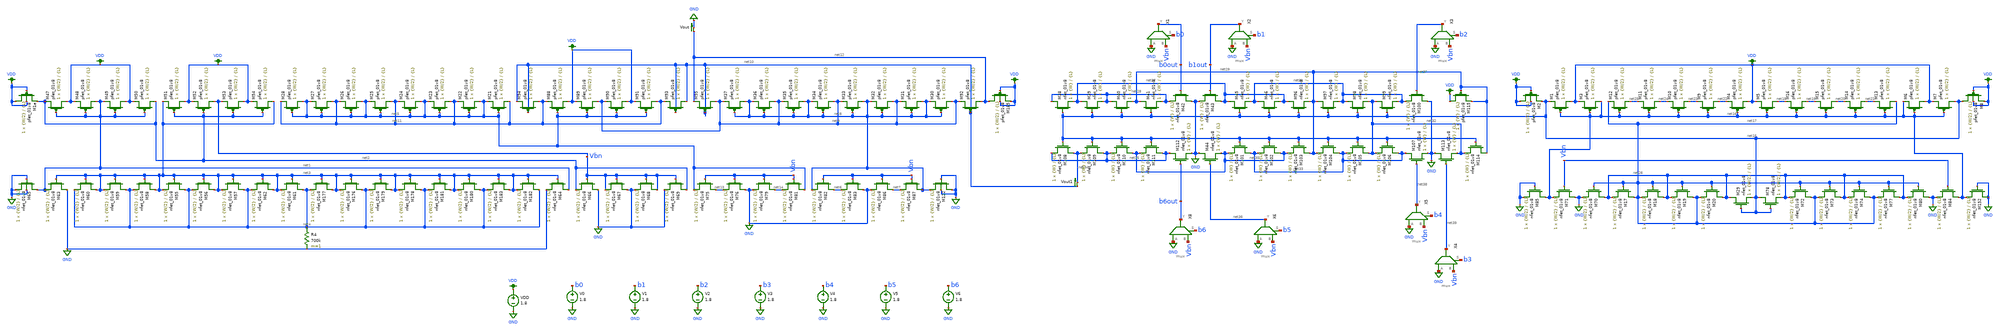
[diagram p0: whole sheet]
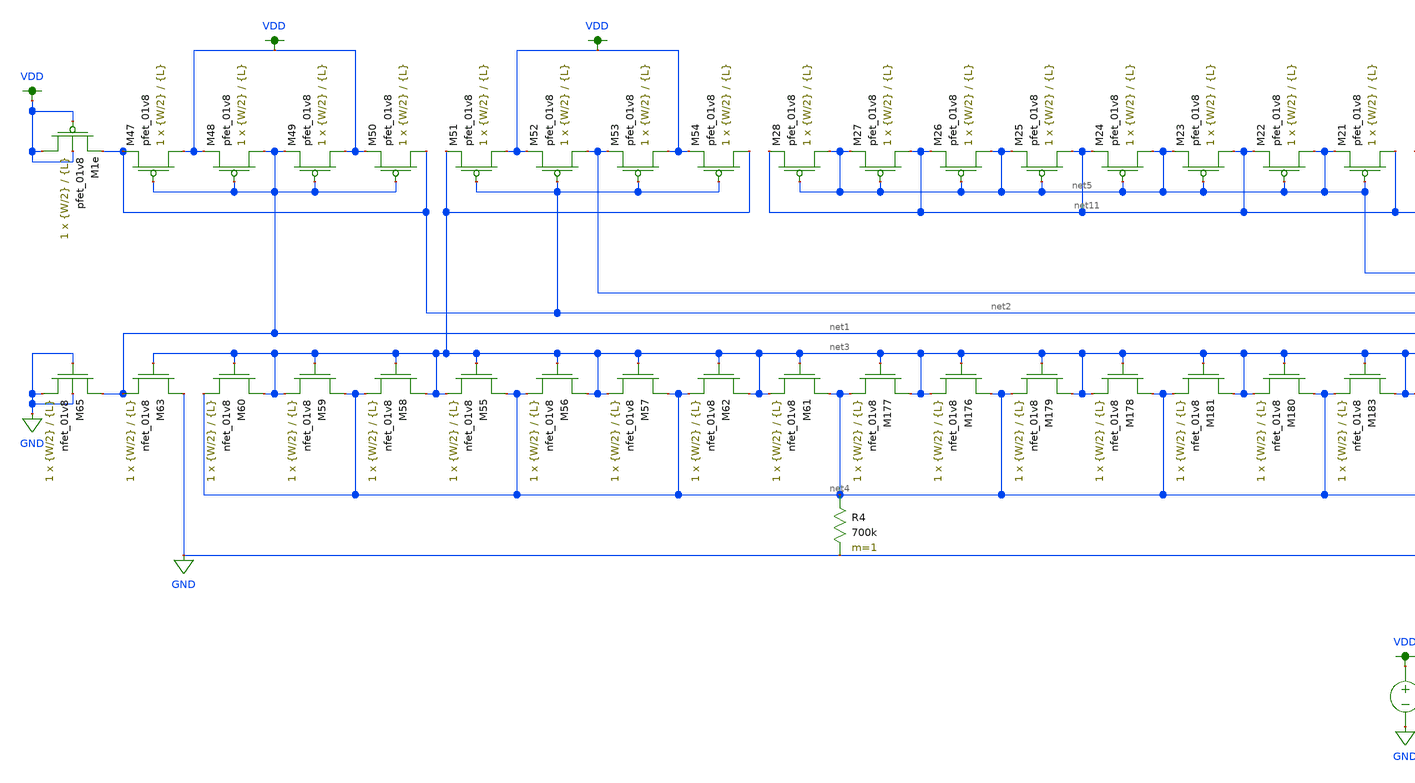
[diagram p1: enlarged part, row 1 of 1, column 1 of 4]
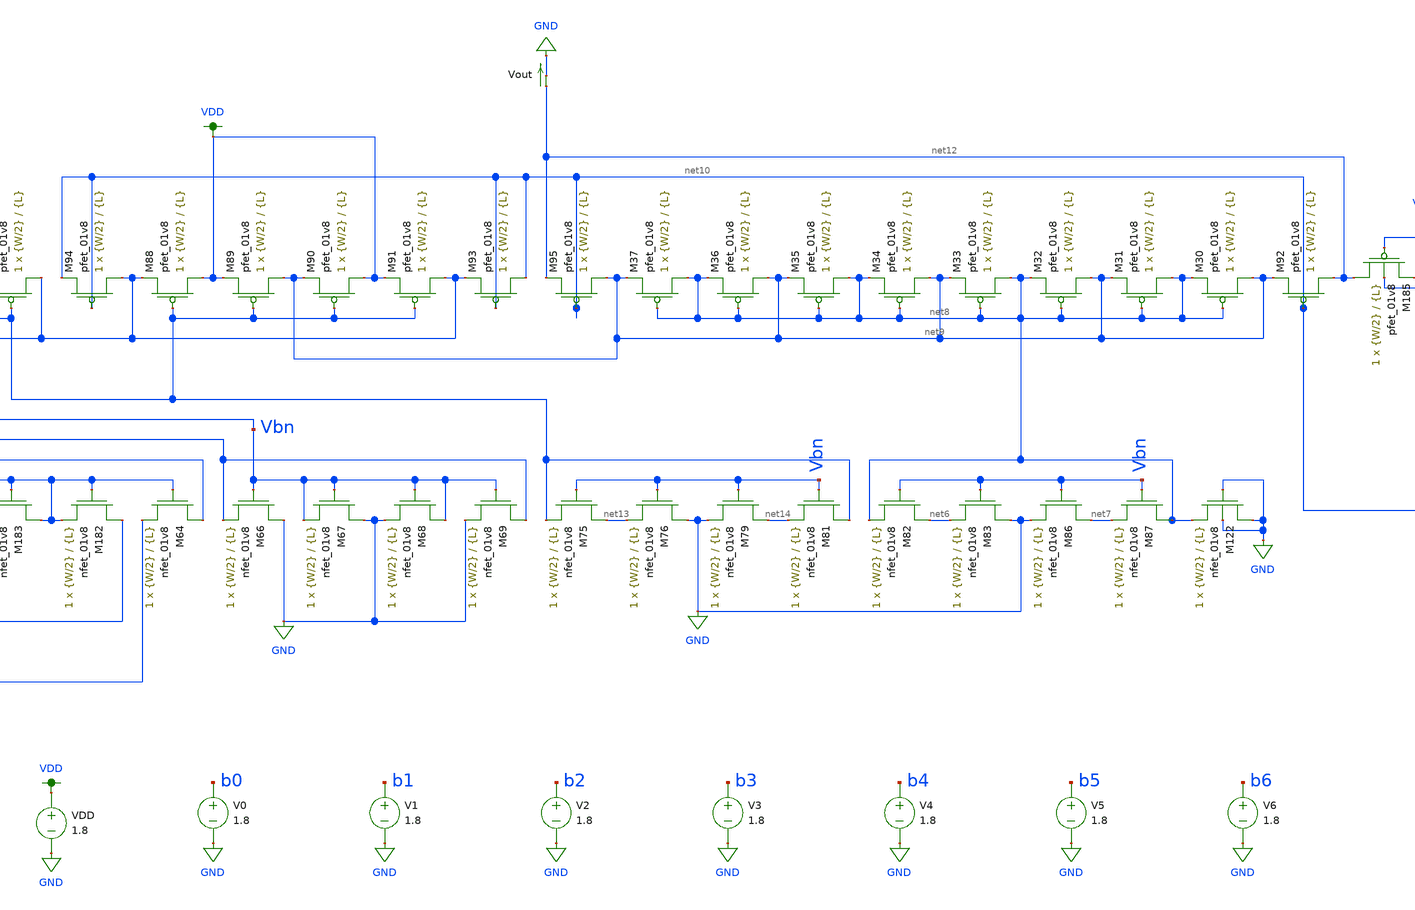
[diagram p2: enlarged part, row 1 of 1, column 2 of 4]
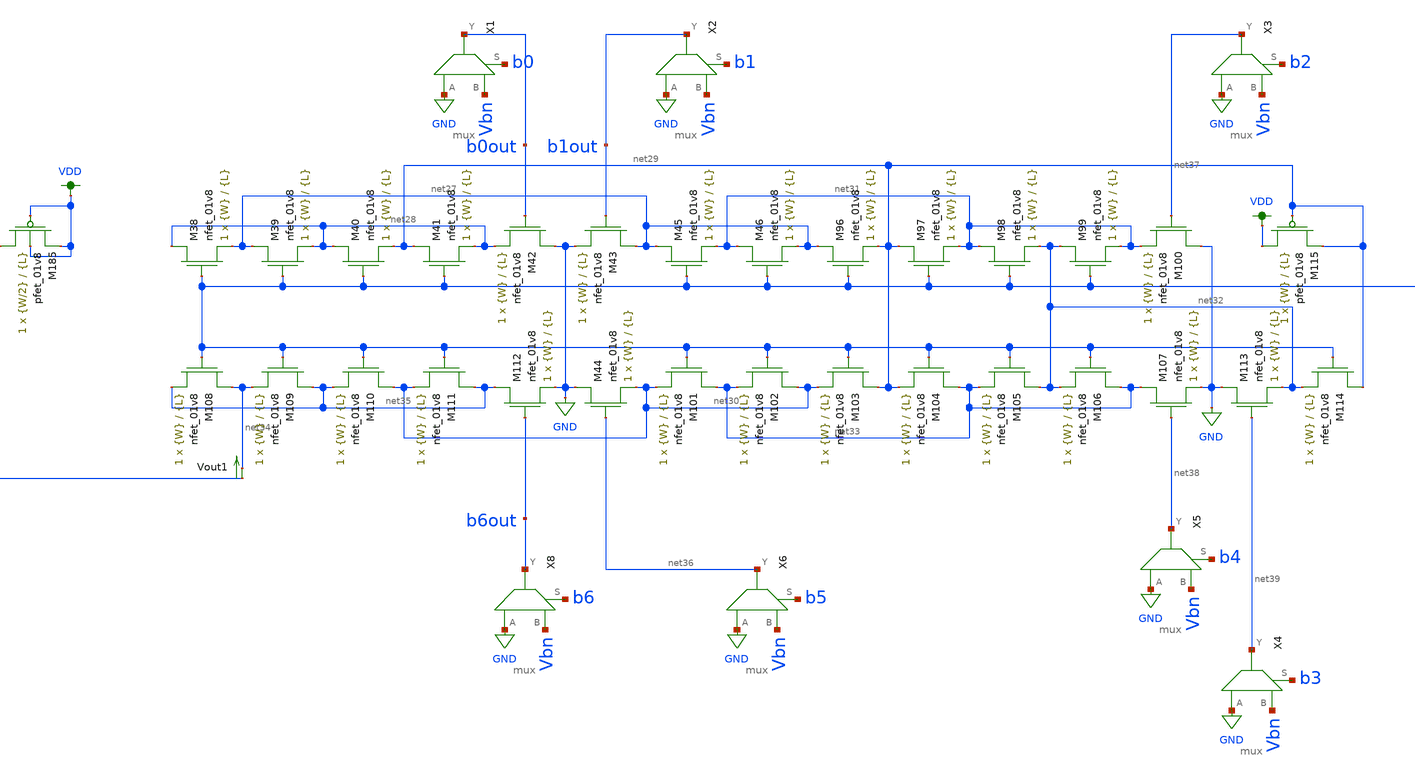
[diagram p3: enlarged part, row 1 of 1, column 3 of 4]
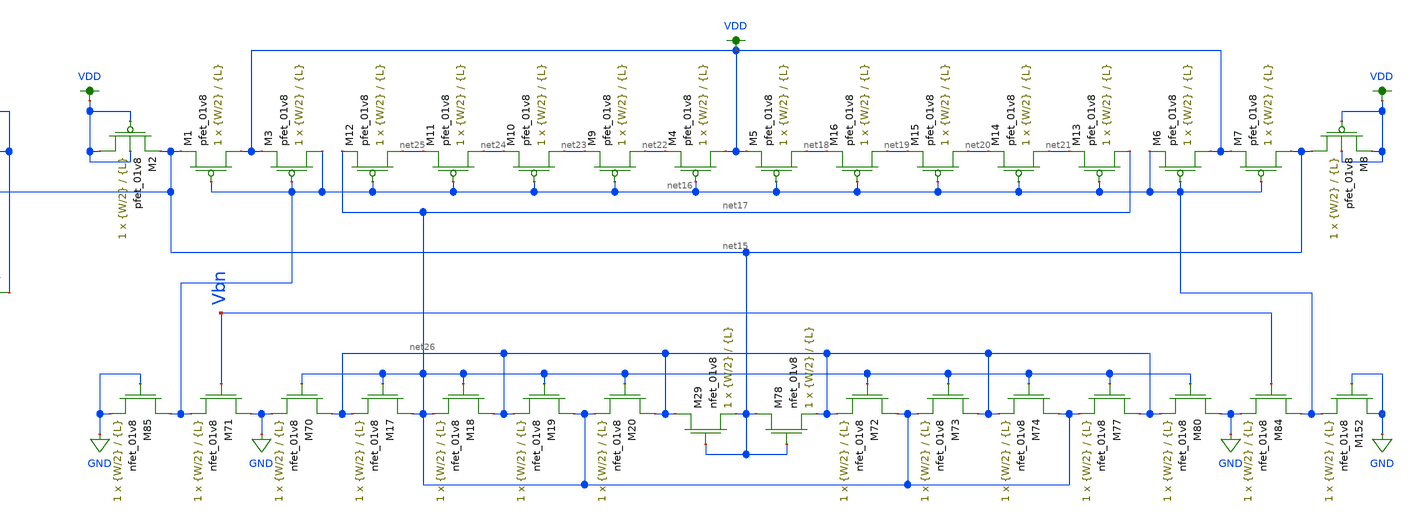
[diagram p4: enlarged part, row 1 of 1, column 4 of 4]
** sch_path: dac/schematics/LDS_FINAL_MONTE_CARLO.sch
**.subckt LDS_FINAL_MONTE_CARLO
V0 b0 GND 1.8
V1 b1 GND 1.8
V2 b2 GND 1.8
V3 b3 GND 1.8
V4 b4 GND 1.8
V5 b5 GND 1.8
V6 b6 GND 1.8
VDD VDD GND 1.8
XM47 VDD net1 net2 VDD sky130_fd_pr__pfet_01v8 L={L} W={W/2} nf=1 ad='int((nf+1)/2) * W/nf * 0.29' as='int((nf+2)/2) * W/nf * 0.29'
+ pd='2*int((nf+1)/2) * (W/nf + 0.29)' ps='2*int((nf+2)/2) * (W/nf + 0.29)' nrd='0.29 / W' nrs='0.29 / W'
+ sa=0 sb=0 sd=0 mult=1 m=1
XM48 net1 net1 VDD VDD sky130_fd_pr__pfet_01v8 L={L} W={W/2} nf=1 ad='int((nf+1)/2) * W/nf * 0.29' as='int((nf+2)/2) * W/nf * 0.29'
+ pd='2*int((nf+1)/2) * (W/nf + 0.29)' ps='2*int((nf+2)/2) * (W/nf + 0.29)' nrd='0.29 / W' nrs='0.29 / W'
+ sa=0 sb=0 sd=0 mult=1 m=1
XM49 VDD net1 net1 VDD sky130_fd_pr__pfet_01v8 L={L} W={W/2} nf=1 ad='int((nf+1)/2) * W/nf * 0.29' as='int((nf+2)/2) * W/nf * 0.29'
+ pd='2*int((nf+1)/2) * (W/nf + 0.29)' ps='2*int((nf+2)/2) * (W/nf + 0.29)' nrd='0.29 / W' nrs='0.29 / W'
+ sa=0 sb=0 sd=0 mult=1 m=1
XM50 net2 net1 VDD VDD sky130_fd_pr__pfet_01v8 L={L} W={W/2} nf=1 ad='int((nf+1)/2) * W/nf * 0.29' as='int((nf+2)/2) * W/nf * 0.29'
+ pd='2*int((nf+1)/2) * (W/nf + 0.29)' ps='2*int((nf+2)/2) * (W/nf + 0.29)' nrd='0.29 / W' nrs='0.29 / W'
+ sa=0 sb=0 sd=0 mult=1 m=1
XM51 VDD net2 net3 VDD sky130_fd_pr__pfet_01v8 L={L} W={W/2} nf=1 ad='int((nf+1)/2) * W/nf * 0.29' as='int((nf+2)/2) * W/nf * 0.29'
+ pd='2*int((nf+1)/2) * (W/nf + 0.29)' ps='2*int((nf+2)/2) * (W/nf + 0.29)' nrd='0.29 / W' nrs='0.29 / W'
+ sa=0 sb=0 sd=0 mult=1 m=1
XM52 Vbn net2 VDD VDD sky130_fd_pr__pfet_01v8 L={L} W={W/2} nf=1 ad='int((nf+1)/2) * W/nf * 0.29' as='int((nf+2)/2) * W/nf * 0.29'
+ pd='2*int((nf+1)/2) * (W/nf + 0.29)' ps='2*int((nf+2)/2) * (W/nf + 0.29)' nrd='0.29 / W' nrs='0.29 / W'
+ sa=0 sb=0 sd=0 mult=1 m=1
XM53 VDD net2 Vbn VDD sky130_fd_pr__pfet_01v8 L={L} W={W/2} nf=1 ad='int((nf+1)/2) * W/nf * 0.29' as='int((nf+2)/2) * W/nf * 0.29'
+ pd='2*int((nf+1)/2) * (W/nf + 0.29)' ps='2*int((nf+2)/2) * (W/nf + 0.29)' nrd='0.29 / W' nrs='0.29 / W'
+ sa=0 sb=0 sd=0 mult=1 m=1
XM54 net3 net2 VDD VDD sky130_fd_pr__pfet_01v8 L={L} W={W/2} nf=1 ad='int((nf+1)/2) * W/nf * 0.29' as='int((nf+2)/2) * W/nf * 0.29'
+ pd='2*int((nf+1)/2) * (W/nf + 0.29)' ps='2*int((nf+2)/2) * (W/nf + 0.29)' nrd='0.29 / W' nrs='0.29 / W'
+ sa=0 sb=0 sd=0 mult=1 m=1
XM55 net4 net3 net3 GND sky130_fd_pr__nfet_01v8 L={L} W={W/2} nf=1 ad='int((nf+1)/2) * W/nf * 0.29' as='int((nf+2)/2) * W/nf * 0.29'
+ pd='2*int((nf+1)/2) * (W/nf + 0.29)' ps='2*int((nf+2)/2) * (W/nf + 0.29)' nrd='0.29 / W' nrs='0.29 / W'
+ sa=0 sb=0 sd=0 mult=1 m=1
XM56 net3 net3 net4 GND sky130_fd_pr__nfet_01v8 L={L} W={W/2} nf=1 ad='int((nf+1)/2) * W/nf * 0.29' as='int((nf+2)/2) * W/nf * 0.29'
+ pd='2*int((nf+1)/2) * (W/nf + 0.29)' ps='2*int((nf+2)/2) * (W/nf + 0.29)' nrd='0.29 / W' nrs='0.29 / W'
+ sa=0 sb=0 sd=0 mult=1 m=1
XM57 net4 net3 net3 GND sky130_fd_pr__nfet_01v8 L={L} W={W/2} nf=1 ad='int((nf+1)/2) * W/nf * 0.29' as='int((nf+2)/2) * W/nf * 0.29'
+ pd='2*int((nf+1)/2) * (W/nf + 0.29)' ps='2*int((nf+2)/2) * (W/nf + 0.29)' nrd='0.29 / W' nrs='0.29 / W'
+ sa=0 sb=0 sd=0 mult=1 m=1
XM58 net3 net3 net4 GND sky130_fd_pr__nfet_01v8 L={L} W={W/2} nf=1 ad='int((nf+1)/2) * W/nf * 0.29' as='int((nf+2)/2) * W/nf * 0.29'
+ pd='2*int((nf+1)/2) * (W/nf + 0.29)' ps='2*int((nf+2)/2) * (W/nf + 0.29)' nrd='0.29 / W' nrs='0.29 / W'
+ sa=0 sb=0 sd=0 mult=1 m=1
XM59 net4 net3 net3 GND sky130_fd_pr__nfet_01v8 L={L} W={W/2} nf=1 ad='int((nf+1)/2) * W/nf * 0.29' as='int((nf+2)/2) * W/nf * 0.29'
+ pd='2*int((nf+1)/2) * (W/nf + 0.29)' ps='2*int((nf+2)/2) * (W/nf + 0.29)' nrd='0.29 / W' nrs='0.29 / W'
+ sa=0 sb=0 sd=0 mult=1 m=1
XM60 net3 net3 net4 GND sky130_fd_pr__nfet_01v8 L={L} W={W/2} nf=1 ad='int((nf+1)/2) * W/nf * 0.29' as='int((nf+2)/2) * W/nf * 0.29'
+ pd='2*int((nf+1)/2) * (W/nf + 0.29)' ps='2*int((nf+2)/2) * (W/nf + 0.29)' nrd='0.29 / W' nrs='0.29 / W'
+ sa=0 sb=0 sd=0 mult=1 m=1
XM61 net4 net3 net3 GND sky130_fd_pr__nfet_01v8 L={L} W={W/2} nf=1 ad='int((nf+1)/2) * W/nf * 0.29' as='int((nf+2)/2) * W/nf * 0.29'
+ pd='2*int((nf+1)/2) * (W/nf + 0.29)' ps='2*int((nf+2)/2) * (W/nf + 0.29)' nrd='0.29 / W' nrs='0.29 / W'
+ sa=0 sb=0 sd=0 mult=1 m=1
XM62 net3 net3 net4 GND sky130_fd_pr__nfet_01v8 L={L} W={W/2} nf=1 ad='int((nf+1)/2) * W/nf * 0.29' as='int((nf+2)/2) * W/nf * 0.29'
+ pd='2*int((nf+1)/2) * (W/nf + 0.29)' ps='2*int((nf+2)/2) * (W/nf + 0.29)' nrd='0.29 / W' nrs='0.29 / W'
+ sa=0 sb=0 sd=0 mult=1 m=1
XM63 GND net3 net1 GND sky130_fd_pr__nfet_01v8 L={L} W={W/2} nf=1 ad='int((nf+1)/2) * W/nf * 0.29' as='int((nf+2)/2) * W/nf * 0.29'
+ pd='2*int((nf+1)/2) * (W/nf + 0.29)' ps='2*int((nf+2)/2) * (W/nf + 0.29)' nrd='0.29 / W' nrs='0.29 / W'
+ sa=0 sb=0 sd=0 mult=1 m=1
XM64 net1 net3 GND GND sky130_fd_pr__nfet_01v8 L={L} W={W/2} nf=1 ad='int((nf+1)/2) * W/nf * 0.29' as='int((nf+2)/2) * W/nf * 0.29'
+ pd='2*int((nf+1)/2) * (W/nf + 0.29)' ps='2*int((nf+2)/2) * (W/nf + 0.29)' nrd='0.29 / W' nrs='0.29 / W'
+ sa=0 sb=0 sd=0 mult=1 m=1
R4 net4 GND 700k m=1
XM1e VDD VDD net2 VDD sky130_fd_pr__pfet_01v8 L={L} W={W/2} nf=1 ad='int((nf+1)/2) * W/nf * 0.29' as='int((nf+2)/2) * W/nf * 0.29'
+ pd='2*int((nf+1)/2) * (W/nf + 0.29)' ps='2*int((nf+2)/2) * (W/nf + 0.29)' nrd='0.29 / W' nrs='0.29 / W'
+ sa=0 sb=0 sd=0 mult=1 m=1
XM65 net1 GND GND GND sky130_fd_pr__nfet_01v8 L={L} W={W/2} nf=1 ad='int((nf+1)/2) * W/nf * 0.29' as='int((nf+2)/2) * W/nf * 0.29'
+ pd='2*int((nf+1)/2) * (W/nf + 0.29)' ps='2*int((nf+2)/2) * (W/nf + 0.29)' nrd='0.29 / W' nrs='0.29 / W'
+ sa=0 sb=0 sd=0 mult=1 m=1
XM66 GND Vbn net2 GND sky130_fd_pr__nfet_01v8 L={L} W={W/2} nf=1 ad='int((nf+1)/2) * W/nf * 0.29' as='int((nf+2)/2) * W/nf * 0.29'
+ pd='2*int((nf+1)/2) * (W/nf + 0.29)' ps='2*int((nf+2)/2) * (W/nf + 0.29)' nrd='0.29 / W' nrs='0.29 / W'
+ sa=0 sb=0 sd=0 mult=1 m=1
XM67 GND Vbn Vbn GND sky130_fd_pr__nfet_01v8 L={L} W={W/2} nf=1 ad='int((nf+1)/2) * W/nf * 0.29' as='int((nf+2)/2) * W/nf * 0.29'
+ pd='2*int((nf+1)/2) * (W/nf + 0.29)' ps='2*int((nf+2)/2) * (W/nf + 0.29)' nrd='0.29 / W' nrs='0.29 / W'
+ sa=0 sb=0 sd=0 mult=1 m=1
XM68 Vbn Vbn GND GND sky130_fd_pr__nfet_01v8 L={L} W={W/2} nf=1 ad='int((nf+1)/2) * W/nf * 0.29' as='int((nf+2)/2) * W/nf * 0.29'
+ pd='2*int((nf+1)/2) * (W/nf + 0.29)' ps='2*int((nf+2)/2) * (W/nf + 0.29)' nrd='0.29 / W' nrs='0.29 / W'
+ sa=0 sb=0 sd=0 mult=1 m=1
XM69 net2 Vbn GND GND sky130_fd_pr__nfet_01v8 L={L} W={W/2} nf=1 ad='int((nf+1)/2) * W/nf * 0.29' as='int((nf+2)/2) * W/nf * 0.29'
+ pd='2*int((nf+1)/2) * (W/nf + 0.29)' ps='2*int((nf+2)/2) * (W/nf + 0.29)' nrd='0.29 / W' nrs='0.29 / W'
+ sa=0 sb=0 sd=0 mult=1 m=1
XM75 net13 Vbn net5 GND sky130_fd_pr__nfet_01v8 L={L} W={W/2} nf=1 ad='int((nf+1)/2) * W/nf * 0.29' as='int((nf+2)/2) * W/nf * 0.29'
+ pd='2*int((nf+1)/2) * (W/nf + 0.29)' ps='2*int((nf+2)/2) * (W/nf + 0.29)' nrd='0.29 / W' nrs='0.29 / W'
+ sa=0 sb=0 sd=0 mult=1 m=1
XM76 GND Vbn net13 GND sky130_fd_pr__nfet_01v8 L={L} W={W/2} nf=1 ad='int((nf+1)/2) * W/nf * 0.29' as='int((nf+2)/2) * W/nf * 0.29'
+ pd='2*int((nf+1)/2) * (W/nf + 0.29)' ps='2*int((nf+2)/2) * (W/nf + 0.29)' nrd='0.29 / W' nrs='0.29 / W'
+ sa=0 sb=0 sd=0 mult=1 m=1
XM79 net14 Vbn GND GND sky130_fd_pr__nfet_01v8 L={L} W={W/2} nf=1 ad='int((nf+1)/2) * W/nf * 0.29' as='int((nf+2)/2) * W/nf * 0.29'
+ pd='2*int((nf+1)/2) * (W/nf + 0.29)' ps='2*int((nf+2)/2) * (W/nf + 0.29)' nrd='0.29 / W' nrs='0.29 / W'
+ sa=0 sb=0 sd=0 mult=1 m=1
XM81 net5 Vbn net14 GND sky130_fd_pr__nfet_01v8 L={L} W={W/2} nf=1 ad='int((nf+1)/2) * W/nf * 0.29' as='int((nf+2)/2) * W/nf * 0.29'
+ pd='2*int((nf+1)/2) * (W/nf + 0.29)' ps='2*int((nf+2)/2) * (W/nf + 0.29)' nrd='0.29 / W' nrs='0.29 / W'
+ sa=0 sb=0 sd=0 mult=1 m=1
XM82 net6 Vbn net8 GND sky130_fd_pr__nfet_01v8 L={L} W={W/2} nf=1 ad='int((nf+1)/2) * W/nf * 0.29' as='int((nf+2)/2) * W/nf * 0.29'
+ pd='2*int((nf+1)/2) * (W/nf + 0.29)' ps='2*int((nf+2)/2) * (W/nf + 0.29)' nrd='0.29 / W' nrs='0.29 / W'
+ sa=0 sb=0 sd=0 mult=1 m=1
XM83 GND Vbn net6 GND sky130_fd_pr__nfet_01v8 L={L} W={W/2} nf=1 ad='int((nf+1)/2) * W/nf * 0.29' as='int((nf+2)/2) * W/nf * 0.29'
+ pd='2*int((nf+1)/2) * (W/nf + 0.29)' ps='2*int((nf+2)/2) * (W/nf + 0.29)' nrd='0.29 / W' nrs='0.29 / W'
+ sa=0 sb=0 sd=0 mult=1 m=1
XM86 net7 Vbn GND GND sky130_fd_pr__nfet_01v8 L={L} W={W/2} nf=1 ad='int((nf+1)/2) * W/nf * 0.29' as='int((nf+2)/2) * W/nf * 0.29'
+ pd='2*int((nf+1)/2) * (W/nf + 0.29)' ps='2*int((nf+2)/2) * (W/nf + 0.29)' nrd='0.29 / W' nrs='0.29 / W'
+ sa=0 sb=0 sd=0 mult=1 m=1
XM87 net8 Vbn net7 GND sky130_fd_pr__nfet_01v8 L={L} W={W/2} nf=1 ad='int((nf+1)/2) * W/nf * 0.29' as='int((nf+2)/2) * W/nf * 0.29'
+ pd='2*int((nf+1)/2) * (W/nf + 0.29)' ps='2*int((nf+2)/2) * (W/nf + 0.29)' nrd='0.29 / W' nrs='0.29 / W'
+ sa=0 sb=0 sd=0 mult=1 m=1
XM88 VDD net5 net11 VDD sky130_fd_pr__pfet_01v8 L={L} W={W/2} nf=1 ad='int((nf+1)/2) * W/nf * 0.29' as='int((nf+2)/2) * W/nf * 0.29'
+ pd='2*int((nf+1)/2) * (W/nf + 0.29)' ps='2*int((nf+2)/2) * (W/nf + 0.29)' nrd='0.29 / W' nrs='0.29 / W'
+ sa=0 sb=0 sd=0 mult=1 m=1
XM89 net9 net5 VDD VDD sky130_fd_pr__pfet_01v8 L={L} W={W/2} nf=1 ad='int((nf+1)/2) * W/nf * 0.29' as='int((nf+2)/2) * W/nf * 0.29'
+ pd='2*int((nf+1)/2) * (W/nf + 0.29)' ps='2*int((nf+2)/2) * (W/nf + 0.29)' nrd='0.29 / W' nrs='0.29 / W'
+ sa=0 sb=0 sd=0 mult=1 m=1
XM90 VDD net5 net9 VDD sky130_fd_pr__pfet_01v8 L={L} W={W/2} nf=1 ad='int((nf+1)/2) * W/nf * 0.29' as='int((nf+2)/2) * W/nf * 0.29'
+ pd='2*int((nf+1)/2) * (W/nf + 0.29)' ps='2*int((nf+2)/2) * (W/nf + 0.29)' nrd='0.29 / W' nrs='0.29 / W'
+ sa=0 sb=0 sd=0 mult=1 m=1
XM91 net11 net5 VDD VDD sky130_fd_pr__pfet_01v8 L={L} W={W/2} nf=1 ad='int((nf+1)/2) * W/nf * 0.29' as='int((nf+2)/2) * W/nf * 0.29'
+ pd='2*int((nf+1)/2) * (W/nf + 0.29)' ps='2*int((nf+2)/2) * (W/nf + 0.29)' nrd='0.29 / W' nrs='0.29 / W'
+ sa=0 sb=0 sd=0 mult=1 m=1
XM92 net12 net10 net9 VDD sky130_fd_pr__pfet_01v8 L={L} W={W/2} nf=1 ad='int((nf+1)/2) * W/nf * 0.29'
+ as='int((nf+2)/2) * W/nf * 0.29' pd='2*int((nf+1)/2) * (W/nf + 0.29)' ps='2*int((nf+2)/2) * (W/nf + 0.29)'
+ nrd='0.29 / W' nrs='0.29 / W' sa=0 sb=0 sd=0 mult=1 m=1
XM93 net10 net10 net11 VDD sky130_fd_pr__pfet_01v8 L={L} W={W/2} nf=1 ad='int((nf+1)/2) * W/nf * 0.29'
+ as='int((nf+2)/2) * W/nf * 0.29' pd='2*int((nf+1)/2) * (W/nf + 0.29)' ps='2*int((nf+2)/2) * (W/nf + 0.29)'
+ nrd='0.29 / W' nrs='0.29 / W' sa=0 sb=0 sd=0 mult=1 m=1
XM94 net11 net10 net10 VDD sky130_fd_pr__pfet_01v8 L={L} W={W/2} nf=1 ad='int((nf+1)/2) * W/nf * 0.29'
+ as='int((nf+2)/2) * W/nf * 0.29' pd='2*int((nf+1)/2) * (W/nf + 0.29)' ps='2*int((nf+2)/2) * (W/nf + 0.29)'
+ nrd='0.29 / W' nrs='0.29 / W' sa=0 sb=0 sd=0 mult=1 m=1
XM95 net9 net10 net12 VDD sky130_fd_pr__pfet_01v8 L={L} W={W/2} nf=1 ad='int((nf+1)/2) * W/nf * 0.29'
+ as='int((nf+2)/2) * W/nf * 0.29' pd='2*int((nf+1)/2) * (W/nf + 0.29)' ps='2*int((nf+2)/2) * (W/nf + 0.29)'
+ nrd='0.29 / W' nrs='0.29 / W' sa=0 sb=0 sd=0 mult=1 m=1
XM176 net4 net3 net3 GND sky130_fd_pr__nfet_01v8 L={L} W={W/2} nf=1 ad='int((nf+1)/2) * W/nf * 0.29'
+ as='int((nf+2)/2) * W/nf * 0.29' pd='2*int((nf+1)/2) * (W/nf + 0.29)' ps='2*int((nf+2)/2) * (W/nf + 0.29)'
+ nrd='0.29 / W' nrs='0.29 / W' sa=0 sb=0 sd=0 mult=1 m=1
XM177 net3 net3 net4 GND sky130_fd_pr__nfet_01v8 L={L} W={W/2} nf=1 ad='int((nf+1)/2) * W/nf * 0.29'
+ as='int((nf+2)/2) * W/nf * 0.29' pd='2*int((nf+1)/2) * (W/nf + 0.29)' ps='2*int((nf+2)/2) * (W/nf + 0.29)'
+ nrd='0.29 / W' nrs='0.29 / W' sa=0 sb=0 sd=0 mult=1 m=1
XM178 net4 net3 net3 GND sky130_fd_pr__nfet_01v8 L={L} W={W/2} nf=1 ad='int((nf+1)/2) * W/nf * 0.29'
+ as='int((nf+2)/2) * W/nf * 0.29' pd='2*int((nf+1)/2) * (W/nf + 0.29)' ps='2*int((nf+2)/2) * (W/nf + 0.29)'
+ nrd='0.29 / W' nrs='0.29 / W' sa=0 sb=0 sd=0 mult=1 m=1
XM179 net3 net3 net4 GND sky130_fd_pr__nfet_01v8 L={L} W={W/2} nf=1 ad='int((nf+1)/2) * W/nf * 0.29'
+ as='int((nf+2)/2) * W/nf * 0.29' pd='2*int((nf+1)/2) * (W/nf + 0.29)' ps='2*int((nf+2)/2) * (W/nf + 0.29)'
+ nrd='0.29 / W' nrs='0.29 / W' sa=0 sb=0 sd=0 mult=1 m=1
XM180 net4 net3 net3 GND sky130_fd_pr__nfet_01v8 L={L} W={W/2} nf=1 ad='int((nf+1)/2) * W/nf * 0.29'
+ as='int((nf+2)/2) * W/nf * 0.29' pd='2*int((nf+1)/2) * (W/nf + 0.29)' ps='2*int((nf+2)/2) * (W/nf + 0.29)'
+ nrd='0.29 / W' nrs='0.29 / W' sa=0 sb=0 sd=0 mult=1 m=1
XM181 net3 net3 net4 GND sky130_fd_pr__nfet_01v8 L={L} W={W/2} nf=1 ad='int((nf+1)/2) * W/nf * 0.29'
+ as='int((nf+2)/2) * W/nf * 0.29' pd='2*int((nf+1)/2) * (W/nf + 0.29)' ps='2*int((nf+2)/2) * (W/nf + 0.29)'
+ nrd='0.29 / W' nrs='0.29 / W' sa=0 sb=0 sd=0 mult=1 m=1
XM182 net4 net3 net3 GND sky130_fd_pr__nfet_01v8 L={L} W={W/2} nf=1 ad='int((nf+1)/2) * W/nf * 0.29'
+ as='int((nf+2)/2) * W/nf * 0.29' pd='2*int((nf+1)/2) * (W/nf + 0.29)' ps='2*int((nf+2)/2) * (W/nf + 0.29)'
+ nrd='0.29 / W' nrs='0.29 / W' sa=0 sb=0 sd=0 mult=1 m=1
XM183 net3 net3 net4 GND sky130_fd_pr__nfet_01v8 L={L} W={W/2} nf=1 ad='int((nf+1)/2) * W/nf * 0.29'
+ as='int((nf+2)/2) * W/nf * 0.29' pd='2*int((nf+1)/2) * (W/nf + 0.29)' ps='2*int((nf+2)/2) * (W/nf + 0.29)'
+ nrd='0.29 / W' nrs='0.29 / W' sa=0 sb=0 sd=0 mult=1 m=1
XM185 net12 VDD VDD VDD sky130_fd_pr__pfet_01v8 L={L} W={W/2} nf=1 ad='int((nf+1)/2) * W/nf * 0.29' as='int((nf+2)/2) * W/nf * 0.29'
+ pd='2*int((nf+1)/2) * (W/nf + 0.29)' ps='2*int((nf+2)/2) * (W/nf + 0.29)' nrd='0.29 / W' nrs='0.29 / W'
+ sa=0 sb=0 sd=0 mult=1 m=1
Vout net12 GND 0
.save i(vout)
XM21 net11 net5 net5 VDD sky130_fd_pr__pfet_01v8 L={L} W={W/2} nf=1 ad='int((nf+1)/2) * W/nf * 0.29'
+ as='int((nf+2)/2) * W/nf * 0.29' pd='2*int((nf+1)/2) * (W/nf + 0.29)' ps='2*int((nf+2)/2) * (W/nf + 0.29)'
+ nrd='0.29 / W' nrs='0.29 / W' sa=0 sb=0 sd=0 mult=1 m=1
XM22 net5 net5 net11 VDD sky130_fd_pr__pfet_01v8 L={L} W={W/2} nf=1 ad='int((nf+1)/2) * W/nf * 0.29'
+ as='int((nf+2)/2) * W/nf * 0.29' pd='2*int((nf+1)/2) * (W/nf + 0.29)' ps='2*int((nf+2)/2) * (W/nf + 0.29)'
+ nrd='0.29 / W' nrs='0.29 / W' sa=0 sb=0 sd=0 mult=1 m=1
XM23 net11 net5 net5 VDD sky130_fd_pr__pfet_01v8 L={L} W={W/2} nf=1 ad='int((nf+1)/2) * W/nf * 0.29'
+ as='int((nf+2)/2) * W/nf * 0.29' pd='2*int((nf+1)/2) * (W/nf + 0.29)' ps='2*int((nf+2)/2) * (W/nf + 0.29)'
+ nrd='0.29 / W' nrs='0.29 / W' sa=0 sb=0 sd=0 mult=1 m=1
XM24 net5 net5 net11 VDD sky130_fd_pr__pfet_01v8 L={L} W={W/2} nf=1 ad='int((nf+1)/2) * W/nf * 0.29'
+ as='int((nf+2)/2) * W/nf * 0.29' pd='2*int((nf+1)/2) * (W/nf + 0.29)' ps='2*int((nf+2)/2) * (W/nf + 0.29)'
+ nrd='0.29 / W' nrs='0.29 / W' sa=0 sb=0 sd=0 mult=1 m=1
XM25 net11 net5 net5 VDD sky130_fd_pr__pfet_01v8 L={L} W={W/2} nf=1 ad='int((nf+1)/2) * W/nf * 0.29'
+ as='int((nf+2)/2) * W/nf * 0.29' pd='2*int((nf+1)/2) * (W/nf + 0.29)' ps='2*int((nf+2)/2) * (W/nf + 0.29)'
+ nrd='0.29 / W' nrs='0.29 / W' sa=0 sb=0 sd=0 mult=1 m=1
XM26 net5 net5 net11 VDD sky130_fd_pr__pfet_01v8 L={L} W={W/2} nf=1 ad='int((nf+1)/2) * W/nf * 0.29'
+ as='int((nf+2)/2) * W/nf * 0.29' pd='2*int((nf+1)/2) * (W/nf + 0.29)' ps='2*int((nf+2)/2) * (W/nf + 0.29)'
+ nrd='0.29 / W' nrs='0.29 / W' sa=0 sb=0 sd=0 mult=1 m=1
XM27 net11 net5 net5 VDD sky130_fd_pr__pfet_01v8 L={L} W={W/2} nf=1 ad='int((nf+1)/2) * W/nf * 0.29'
+ as='int((nf+2)/2) * W/nf * 0.29' pd='2*int((nf+1)/2) * (W/nf + 0.29)' ps='2*int((nf+2)/2) * (W/nf + 0.29)'
+ nrd='0.29 / W' nrs='0.29 / W' sa=0 sb=0 sd=0 mult=1 m=1
XM28 net5 net5 net11 VDD sky130_fd_pr__pfet_01v8 L={L} W={W/2} nf=1 ad='int((nf+1)/2) * W/nf * 0.29'
+ as='int((nf+2)/2) * W/nf * 0.29' pd='2*int((nf+1)/2) * (W/nf + 0.29)' ps='2*int((nf+2)/2) * (W/nf + 0.29)'
+ nrd='0.29 / W' nrs='0.29 / W' sa=0 sb=0 sd=0 mult=1 m=1
XM30 net9 net8 net8 VDD sky130_fd_pr__pfet_01v8 L={L} W={W/2} nf=1 ad='int((nf+1)/2) * W/nf * 0.29' as='int((nf+2)/2) * W/nf * 0.29'
+ pd='2*int((nf+1)/2) * (W/nf + 0.29)' ps='2*int((nf+2)/2) * (W/nf + 0.29)' nrd='0.29 / W' nrs='0.29 / W'
+ sa=0 sb=0 sd=0 mult=1 m=1
XM31 net8 net8 net9 VDD sky130_fd_pr__pfet_01v8 L={L} W={W/2} nf=1 ad='int((nf+1)/2) * W/nf * 0.29' as='int((nf+2)/2) * W/nf * 0.29'
+ pd='2*int((nf+1)/2) * (W/nf + 0.29)' ps='2*int((nf+2)/2) * (W/nf + 0.29)' nrd='0.29 / W' nrs='0.29 / W'
+ sa=0 sb=0 sd=0 mult=1 m=1
XM32 net9 net8 net8 VDD sky130_fd_pr__pfet_01v8 L={L} W={W/2} nf=1 ad='int((nf+1)/2) * W/nf * 0.29' as='int((nf+2)/2) * W/nf * 0.29'
+ pd='2*int((nf+1)/2) * (W/nf + 0.29)' ps='2*int((nf+2)/2) * (W/nf + 0.29)' nrd='0.29 / W' nrs='0.29 / W'
+ sa=0 sb=0 sd=0 mult=1 m=1
XM33 net8 net8 net9 VDD sky130_fd_pr__pfet_01v8 L={L} W={W/2} nf=1 ad='int((nf+1)/2) * W/nf * 0.29' as='int((nf+2)/2) * W/nf * 0.29'
+ pd='2*int((nf+1)/2) * (W/nf + 0.29)' ps='2*int((nf+2)/2) * (W/nf + 0.29)' nrd='0.29 / W' nrs='0.29 / W'
+ sa=0 sb=0 sd=0 mult=1 m=1
XM34 net9 net8 net8 VDD sky130_fd_pr__pfet_01v8 L={L} W={W/2} nf=1 ad='int((nf+1)/2) * W/nf * 0.29' as='int((nf+2)/2) * W/nf * 0.29'
+ pd='2*int((nf+1)/2) * (W/nf + 0.29)' ps='2*int((nf+2)/2) * (W/nf + 0.29)' nrd='0.29 / W' nrs='0.29 / W'
+ sa=0 sb=0 sd=0 mult=1 m=1
XM35 net8 net8 net9 VDD sky130_fd_pr__pfet_01v8 L={L} W={W/2} nf=1 ad='int((nf+1)/2) * W/nf * 0.29' as='int((nf+2)/2) * W/nf * 0.29'
+ pd='2*int((nf+1)/2) * (W/nf + 0.29)' ps='2*int((nf+2)/2) * (W/nf + 0.29)' nrd='0.29 / W' nrs='0.29 / W'
+ sa=0 sb=0 sd=0 mult=1 m=1
XM36 net9 net8 net8 VDD sky130_fd_pr__pfet_01v8 L={L} W={W/2} nf=1 ad='int((nf+1)/2) * W/nf * 0.29' as='int((nf+2)/2) * W/nf * 0.29'
+ pd='2*int((nf+1)/2) * (W/nf + 0.29)' ps='2*int((nf+2)/2) * (W/nf + 0.29)' nrd='0.29 / W' nrs='0.29 / W'
+ sa=0 sb=0 sd=0 mult=1 m=1
XM37 net8 net8 net9 VDD sky130_fd_pr__pfet_01v8 L={L} W={W/2} nf=1 ad='int((nf+1)/2) * W/nf * 0.29' as='int((nf+2)/2) * W/nf * 0.29'
+ pd='2*int((nf+1)/2) * (W/nf + 0.29)' ps='2*int((nf+2)/2) * (W/nf + 0.29)' nrd='0.29 / W' nrs='0.29 / W'
+ sa=0 sb=0 sd=0 mult=1 m=1
XM122 GND GND net8 GND sky130_fd_pr__nfet_01v8 L={L} W={W/2} nf=1 ad='int((nf+1)/2) * W/nf * 0.29' as='int((nf+2)/2) * W/nf * 0.29'
+ pd='2*int((nf+1)/2) * (W/nf + 0.29)' ps='2*int((nf+2)/2) * (W/nf + 0.29)' nrd='0.29 / W' nrs='0.29 / W'
+ sa=0 sb=0 sd=0 mult=1 m=1
XM1 VDD net16 net15 VDD sky130_fd_pr__pfet_01v8 L={L} W={W/2} nf=1 ad='int((nf+1)/2) * W/nf * 0.29' as='int((nf+2)/2) * W/nf * 0.29'
+ pd='2*int((nf+1)/2) * (W/nf + 0.29)' ps='2*int((nf+2)/2) * (W/nf + 0.29)' nrd='0.29 / W' nrs='0.29 / W'
+ sa=0 sb=0 sd=0 mult=1 m=1
XM2 VDD VDD net15 VDD sky130_fd_pr__pfet_01v8 L={L} W={W/2} nf=1 ad='int((nf+1)/2) * W/nf * 0.29' as='int((nf+2)/2) * W/nf * 0.29'
+ pd='2*int((nf+1)/2) * (W/nf + 0.29)' ps='2*int((nf+2)/2) * (W/nf + 0.29)' nrd='0.29 / W' nrs='0.29 / W'
+ sa=0 sb=0 sd=0 mult=1 m=1
XM3 net16 net16 VDD VDD sky130_fd_pr__pfet_01v8 L={L} W={W/2} nf=1 ad='int((nf+1)/2) * W/nf * 0.29' as='int((nf+2)/2) * W/nf * 0.29'
+ pd='2*int((nf+1)/2) * (W/nf + 0.29)' ps='2*int((nf+2)/2) * (W/nf + 0.29)' nrd='0.29 / W' nrs='0.29 / W'
+ sa=0 sb=0 sd=0 mult=1 m=1
XM4 VDD net16 net22 VDD sky130_fd_pr__pfet_01v8 L={L} W={W/2} nf=1 ad='int((nf+1)/2) * W/nf * 0.29' as='int((nf+2)/2) * W/nf * 0.29'
+ pd='2*int((nf+1)/2) * (W/nf + 0.29)' ps='2*int((nf+2)/2) * (W/nf + 0.29)' nrd='0.29 / W' nrs='0.29 / W'
+ sa=0 sb=0 sd=0 mult=1 m=1
XM5 net18 net16 VDD VDD sky130_fd_pr__pfet_01v8 L={L} W={W/2} nf=1 ad='int((nf+1)/2) * W/nf * 0.29' as='int((nf+2)/2) * W/nf * 0.29'
+ pd='2*int((nf+1)/2) * (W/nf + 0.29)' ps='2*int((nf+2)/2) * (W/nf + 0.29)' nrd='0.29 / W' nrs='0.29 / W'
+ sa=0 sb=0 sd=0 mult=1 m=1
XM6 VDD net16 net16 VDD sky130_fd_pr__pfet_01v8 L={L} W={W/2} nf=1 ad='int((nf+1)/2) * W/nf * 0.29' as='int((nf+2)/2) * W/nf * 0.29'
+ pd='2*int((nf+1)/2) * (W/nf + 0.29)' ps='2*int((nf+2)/2) * (W/nf + 0.29)' nrd='0.29 / W' nrs='0.29 / W'
+ sa=0 sb=0 sd=0 mult=1 m=1
XM7 net15 net16 VDD VDD sky130_fd_pr__pfet_01v8 L={L} W={W/2} nf=1 ad='int((nf+1)/2) * W/nf * 0.29' as='int((nf+2)/2) * W/nf * 0.29'
+ pd='2*int((nf+1)/2) * (W/nf + 0.29)' ps='2*int((nf+2)/2) * (W/nf + 0.29)' nrd='0.29 / W' nrs='0.29 / W'
+ sa=0 sb=0 sd=0 mult=1 m=1
XM8 net15 VDD VDD VDD sky130_fd_pr__pfet_01v8 L={L} W={W/2} nf=1 ad='int((nf+1)/2) * W/nf * 0.29' as='int((nf+2)/2) * W/nf * 0.29'
+ pd='2*int((nf+1)/2) * (W/nf + 0.29)' ps='2*int((nf+2)/2) * (W/nf + 0.29)' nrd='0.29 / W' nrs='0.29 / W'
+ sa=0 sb=0 sd=0 mult=1 m=1
XM9 net22 net16 net23 VDD sky130_fd_pr__pfet_01v8 L={L} W={W/2} nf=1 ad='int((nf+1)/2) * W/nf * 0.29'
+ as='int((nf+2)/2) * W/nf * 0.29' pd='2*int((nf+1)/2) * (W/nf + 0.29)' ps='2*int((nf+2)/2) * (W/nf + 0.29)'
+ nrd='0.29 / W' nrs='0.29 / W' sa=0 sb=0 sd=0 mult=1 m=1
XM10 net23 net16 net24 VDD sky130_fd_pr__pfet_01v8 L={L} W={W/2} nf=1 ad='int((nf+1)/2) * W/nf * 0.29'
+ as='int((nf+2)/2) * W/nf * 0.29' pd='2*int((nf+1)/2) * (W/nf + 0.29)' ps='2*int((nf+2)/2) * (W/nf + 0.29)'
+ nrd='0.29 / W' nrs='0.29 / W' sa=0 sb=0 sd=0 mult=1 m=1
XM11 net24 net16 net25 VDD sky130_fd_pr__pfet_01v8 L={L} W={W/2} nf=1 ad='int((nf+1)/2) * W/nf * 0.29'
+ as='int((nf+2)/2) * W/nf * 0.29' pd='2*int((nf+1)/2) * (W/nf + 0.29)' ps='2*int((nf+2)/2) * (W/nf + 0.29)'
+ nrd='0.29 / W' nrs='0.29 / W' sa=0 sb=0 sd=0 mult=1 m=1
XM12 net25 net16 net17 VDD sky130_fd_pr__pfet_01v8 L={L} W={W/2} nf=1 ad='int((nf+1)/2) * W/nf * 0.29'
+ as='int((nf+2)/2) * W/nf * 0.29' pd='2*int((nf+1)/2) * (W/nf + 0.29)' ps='2*int((nf+2)/2) * (W/nf + 0.29)'
+ nrd='0.29 / W' nrs='0.29 / W' sa=0 sb=0 sd=0 mult=1 m=1
XM13 net17 net16 net21 VDD sky130_fd_pr__pfet_01v8 L={L} W={W/2} nf=1 ad='int((nf+1)/2) * W/nf * 0.29'
+ as='int((nf+2)/2) * W/nf * 0.29' pd='2*int((nf+1)/2) * (W/nf + 0.29)' ps='2*int((nf+2)/2) * (W/nf + 0.29)'
+ nrd='0.29 / W' nrs='0.29 / W' sa=0 sb=0 sd=0 mult=1 m=1
XM14 net21 net16 net20 VDD sky130_fd_pr__pfet_01v8 L={L} W={W/2} nf=1 ad='int((nf+1)/2) * W/nf * 0.29'
+ as='int((nf+2)/2) * W/nf * 0.29' pd='2*int((nf+1)/2) * (W/nf + 0.29)' ps='2*int((nf+2)/2) * (W/nf + 0.29)'
+ nrd='0.29 / W' nrs='0.29 / W' sa=0 sb=0 sd=0 mult=1 m=1
XM15 net20 net16 net19 VDD sky130_fd_pr__pfet_01v8 L={L} W={W/2} nf=1 ad='int((nf+1)/2) * W/nf * 0.29'
+ as='int((nf+2)/2) * W/nf * 0.29' pd='2*int((nf+1)/2) * (W/nf + 0.29)' ps='2*int((nf+2)/2) * (W/nf + 0.29)'
+ nrd='0.29 / W' nrs='0.29 / W' sa=0 sb=0 sd=0 mult=1 m=1
XM16 net19 net16 net18 VDD sky130_fd_pr__pfet_01v8 L={L} W={W/2} nf=1 ad='int((nf+1)/2) * W/nf * 0.29'
+ as='int((nf+2)/2) * W/nf * 0.29' pd='2*int((nf+1)/2) * (W/nf + 0.29)' ps='2*int((nf+2)/2) * (W/nf + 0.29)'
+ nrd='0.29 / W' nrs='0.29 / W' sa=0 sb=0 sd=0 mult=1 m=1
XM17 net17 net17 net26 GND sky130_fd_pr__nfet_01v8 L={L} W={W/2} nf=1 ad='int((nf+1)/2) * W/nf * 0.29'
+ as='int((nf+2)/2) * W/nf * 0.29' pd='2*int((nf+1)/2) * (W/nf + 0.29)' ps='2*int((nf+2)/2) * (W/nf + 0.29)'
+ nrd='0.29 / W' nrs='0.29 / W' sa=0 sb=0 sd=0 mult=1 m=1
XM18 net26 net17 net17 GND sky130_fd_pr__nfet_01v8 L={L} W={W/2} nf=1 ad='int((nf+1)/2) * W/nf * 0.29'
+ as='int((nf+2)/2) * W/nf * 0.29' pd='2*int((nf+1)/2) * (W/nf + 0.29)' ps='2*int((nf+2)/2) * (W/nf + 0.29)'
+ nrd='0.29 / W' nrs='0.29 / W' sa=0 sb=0 sd=0 mult=1 m=1
XM19 net17 net17 net26 GND sky130_fd_pr__nfet_01v8 L={L} W={W/2} nf=1 ad='int((nf+1)/2) * W/nf * 0.29'
+ as='int((nf+2)/2) * W/nf * 0.29' pd='2*int((nf+1)/2) * (W/nf + 0.29)' ps='2*int((nf+2)/2) * (W/nf + 0.29)'
+ nrd='0.29 / W' nrs='0.29 / W' sa=0 sb=0 sd=0 mult=1 m=1
XM20 net26 net17 net17 GND sky130_fd_pr__nfet_01v8 L={L} W={W/2} nf=1 ad='int((nf+1)/2) * W/nf * 0.29'
+ as='int((nf+2)/2) * W/nf * 0.29' pd='2*int((nf+1)/2) * (W/nf + 0.29)' ps='2*int((nf+2)/2) * (W/nf + 0.29)'
+ nrd='0.29 / W' nrs='0.29 / W' sa=0 sb=0 sd=0 mult=1 m=1
XM29 net26 net15 net15 GND sky130_fd_pr__nfet_01v8 L={L} W={W/2} nf=1 ad='int((nf+1)/2) * W/nf * 0.29'
+ as='int((nf+2)/2) * W/nf * 0.29' pd='2*int((nf+1)/2) * (W/nf + 0.29)' ps='2*int((nf+2)/2) * (W/nf + 0.29)'
+ nrd='0.29 / W' nrs='0.29 / W' sa=0 sb=0 sd=0 mult=1 m=1
XM70 net26 net17 GND GND sky130_fd_pr__nfet_01v8 L={L} W={W/2} nf=1 ad='int((nf+1)/2) * W/nf * 0.29'
+ as='int((nf+2)/2) * W/nf * 0.29' pd='2*int((nf+1)/2) * (W/nf + 0.29)' ps='2*int((nf+2)/2) * (W/nf + 0.29)'
+ nrd='0.29 / W' nrs='0.29 / W' sa=0 sb=0 sd=0 mult=1 m=1
XM71 GND Vbn net16 GND sky130_fd_pr__nfet_01v8 L={L} W={W/2} nf=1 ad='int((nf+1)/2) * W/nf * 0.29' as='int((nf+2)/2) * W/nf * 0.29'
+ pd='2*int((nf+1)/2) * (W/nf + 0.29)' ps='2*int((nf+2)/2) * (W/nf + 0.29)' nrd='0.29 / W' nrs='0.29 / W'
+ sa=0 sb=0 sd=0 mult=1 m=1
XM72 net17 net17 net26 GND sky130_fd_pr__nfet_01v8 L={L} W={W/2} nf=1 ad='int((nf+1)/2) * W/nf * 0.29'
+ as='int((nf+2)/2) * W/nf * 0.29' pd='2*int((nf+1)/2) * (W/nf + 0.29)' ps='2*int((nf+2)/2) * (W/nf + 0.29)'
+ nrd='0.29 / W' nrs='0.29 / W' sa=0 sb=0 sd=0 mult=1 m=1
XM73 net26 net17 net17 GND sky130_fd_pr__nfet_01v8 L={L} W={W/2} nf=1 ad='int((nf+1)/2) * W/nf * 0.29'
+ as='int((nf+2)/2) * W/nf * 0.29' pd='2*int((nf+1)/2) * (W/nf + 0.29)' ps='2*int((nf+2)/2) * (W/nf + 0.29)'
+ nrd='0.29 / W' nrs='0.29 / W' sa=0 sb=0 sd=0 mult=1 m=1
XM74 net17 net17 net26 GND sky130_fd_pr__nfet_01v8 L={L} W={W/2} nf=1 ad='int((nf+1)/2) * W/nf * 0.29'
+ as='int((nf+2)/2) * W/nf * 0.29' pd='2*int((nf+1)/2) * (W/nf + 0.29)' ps='2*int((nf+2)/2) * (W/nf + 0.29)'
+ nrd='0.29 / W' nrs='0.29 / W' sa=0 sb=0 sd=0 mult=1 m=1
XM77 net26 net17 net17 GND sky130_fd_pr__nfet_01v8 L={L} W={W/2} nf=1 ad='int((nf+1)/2) * W/nf * 0.29'
+ as='int((nf+2)/2) * W/nf * 0.29' pd='2*int((nf+1)/2) * (W/nf + 0.29)' ps='2*int((nf+2)/2) * (W/nf + 0.29)'
+ nrd='0.29 / W' nrs='0.29 / W' sa=0 sb=0 sd=0 mult=1 m=1
XM78 net15 net15 net26 GND sky130_fd_pr__nfet_01v8 L={L} W={W/2} nf=1 ad='int((nf+1)/2) * W/nf * 0.29'
+ as='int((nf+2)/2) * W/nf * 0.29' pd='2*int((nf+1)/2) * (W/nf + 0.29)' ps='2*int((nf+2)/2) * (W/nf + 0.29)'
+ nrd='0.29 / W' nrs='0.29 / W' sa=0 sb=0 sd=0 mult=1 m=1
XM80 GND net17 net26 GND sky130_fd_pr__nfet_01v8 L={L} W={W/2} nf=1 ad='int((nf+1)/2) * W/nf * 0.29'
+ as='int((nf+2)/2) * W/nf * 0.29' pd='2*int((nf+1)/2) * (W/nf + 0.29)' ps='2*int((nf+2)/2) * (W/nf + 0.29)'
+ nrd='0.29 / W' nrs='0.29 / W' sa=0 sb=0 sd=0 mult=1 m=1
XM84 net16 Vbn GND GND sky130_fd_pr__nfet_01v8 L={L} W={W/2} nf=1 ad='int((nf+1)/2) * W/nf * 0.29' as='int((nf+2)/2) * W/nf * 0.29'
+ pd='2*int((nf+1)/2) * (W/nf + 0.29)' ps='2*int((nf+2)/2) * (W/nf + 0.29)' nrd='0.29 / W' nrs='0.29 / W'
+ sa=0 sb=0 sd=0 mult=1 m=1
XM85 net16 GND GND GND sky130_fd_pr__nfet_01v8 L={L} W={W/2} nf=1 ad='int((nf+1)/2) * W/nf * 0.29' as='int((nf+2)/2) * W/nf * 0.29'
+ pd='2*int((nf+1)/2) * (W/nf + 0.29)' ps='2*int((nf+2)/2) * (W/nf + 0.29)' nrd='0.29 / W' nrs='0.29 / W'
+ sa=0 sb=0 sd=0 mult=1 m=1
XM152 GND GND net16 GND sky130_fd_pr__nfet_01v8 L={L} W={W/2} nf=1 ad='int((nf+1)/2) * W/nf * 0.29' as='int((nf+2)/2) * W/nf * 0.29'
+ pd='2*int((nf+1)/2) * (W/nf + 0.29)' ps='2*int((nf+2)/2) * (W/nf + 0.29)' nrd='0.29 / W' nrs='0.29 / W'
+ sa=0 sb=0 sd=0 mult=1 m=1
X1 GND Vbn b0out b0 mux
X2 GND Vbn b1out b1 mux
X3 GND Vbn net37 b2 mux
X4 GND Vbn net39 b3 mux
X5 GND Vbn net38 b4 mux
X6 GND Vbn net36 b5 mux
X8 GND Vbn b6out b6 mux
Vout1 net10 net34 0
.save i(vout1)
XM38 net28 net15 net27 GND sky130_fd_pr__nfet_01v8 L={L} W={W} nf=1 ad='int((nf+1)/2) * W/nf * 0.29'
+ as='int((nf+2)/2) * W/nf * 0.29' pd='2*int((nf+1)/2) * (W/nf + 0.29)' ps='2*int((nf+2)/2) * (W/nf + 0.29)'
+ nrd='0.29 / W' nrs='0.29 / W' sa=0 sb=0 sd=0 mult=1 m=1
XM39 net27 net15 net28 GND sky130_fd_pr__nfet_01v8 L={L} W={W} nf=1 ad='int((nf+1)/2) * W/nf * 0.29'
+ as='int((nf+2)/2) * W/nf * 0.29' pd='2*int((nf+1)/2) * (W/nf + 0.29)' ps='2*int((nf+2)/2) * (W/nf + 0.29)'
+ nrd='0.29 / W' nrs='0.29 / W' sa=0 sb=0 sd=0 mult=1 m=1
XM40 net28 net15 net29 GND sky130_fd_pr__nfet_01v8 L={L} W={W} nf=1 ad='int((nf+1)/2) * W/nf * 0.29'
+ as='int((nf+2)/2) * W/nf * 0.29' pd='2*int((nf+1)/2) * (W/nf + 0.29)' ps='2*int((nf+2)/2) * (W/nf + 0.29)'
+ nrd='0.29 / W' nrs='0.29 / W' sa=0 sb=0 sd=0 mult=1 m=1
XM41 net29 net15 net28 GND sky130_fd_pr__nfet_01v8 L={L} W={W} nf=1 ad='int((nf+1)/2) * W/nf * 0.29'
+ as='int((nf+2)/2) * W/nf * 0.29' pd='2*int((nf+1)/2) * (W/nf + 0.29)' ps='2*int((nf+2)/2) * (W/nf + 0.29)'
+ nrd='0.29 / W' nrs='0.29 / W' sa=0 sb=0 sd=0 mult=1 m=1
XM42 GND b0out net28 GND sky130_fd_pr__nfet_01v8 L={L} W={W} nf=1 ad='int((nf+1)/2) * W/nf * 0.29' as='int((nf+2)/2) * W/nf * 0.29'
+ pd='2*int((nf+1)/2) * (W/nf + 0.29)' ps='2*int((nf+2)/2) * (W/nf + 0.29)' nrd='0.29 / W' nrs='0.29 / W'
+ sa=0 sb=0 sd=0 mult=1 m=1
XM43 net27 b1out GND GND sky130_fd_pr__nfet_01v8 L={L} W={W} nf=1 ad='int((nf+1)/2) * W/nf * 0.29' as='int((nf+2)/2) * W/nf * 0.29'
+ pd='2*int((nf+1)/2) * (W/nf + 0.29)' ps='2*int((nf+2)/2) * (W/nf + 0.29)' nrd='0.29 / W' nrs='0.29 / W'
+ sa=0 sb=0 sd=0 mult=1 m=1
XM44 GND net36 net30 GND sky130_fd_pr__nfet_01v8 L={L} W={W} nf=1 ad='int((nf+1)/2) * W/nf * 0.29' as='int((nf+2)/2) * W/nf * 0.29'
+ pd='2*int((nf+1)/2) * (W/nf + 0.29)' ps='2*int((nf+2)/2) * (W/nf + 0.29)' nrd='0.29 / W' nrs='0.29 / W'
+ sa=0 sb=0 sd=0 mult=1 m=1
XM45 net27 net15 net31 GND sky130_fd_pr__nfet_01v8 L={L} W={W} nf=1 ad='int((nf+1)/2) * W/nf * 0.29'
+ as='int((nf+2)/2) * W/nf * 0.29' pd='2*int((nf+1)/2) * (W/nf + 0.29)' ps='2*int((nf+2)/2) * (W/nf + 0.29)'
+ nrd='0.29 / W' nrs='0.29 / W' sa=0 sb=0 sd=0 mult=1 m=1
XM46 net31 net15 net27 GND sky130_fd_pr__nfet_01v8 L={L} W={W} nf=1 ad='int((nf+1)/2) * W/nf * 0.29'
+ as='int((nf+2)/2) * W/nf * 0.29' pd='2*int((nf+1)/2) * (W/nf + 0.29)' ps='2*int((nf+2)/2) * (W/nf + 0.29)'
+ nrd='0.29 / W' nrs='0.29 / W' sa=0 sb=0 sd=0 mult=1 m=1
XM96 net27 net15 net29 GND sky130_fd_pr__nfet_01v8 L={L} W={W} nf=1 ad='int((nf+1)/2) * W/nf * 0.29'
+ as='int((nf+2)/2) * W/nf * 0.29' pd='2*int((nf+1)/2) * (W/nf + 0.29)' ps='2*int((nf+2)/2) * (W/nf + 0.29)'
+ nrd='0.29 / W' nrs='0.29 / W' sa=0 sb=0 sd=0 mult=1 m=1
XM97 net29 net15 net31 GND sky130_fd_pr__nfet_01v8 L={L} W={W} nf=1 ad='int((nf+1)/2) * W/nf * 0.29'
+ as='int((nf+2)/2) * W/nf * 0.29' pd='2*int((nf+1)/2) * (W/nf + 0.29)' ps='2*int((nf+2)/2) * (W/nf + 0.29)'
+ nrd='0.29 / W' nrs='0.29 / W' sa=0 sb=0 sd=0 mult=1 m=1
XM98 net31 net15 net32 GND sky130_fd_pr__nfet_01v8 L={L} W={W} nf=1 ad='int((nf+1)/2) * W/nf * 0.29'
+ as='int((nf+2)/2) * W/nf * 0.29' pd='2*int((nf+1)/2) * (W/nf + 0.29)' ps='2*int((nf+2)/2) * (W/nf + 0.29)'
+ nrd='0.29 / W' nrs='0.29 / W' sa=0 sb=0 sd=0 mult=1 m=1
XM99 net32 net15 net31 GND sky130_fd_pr__nfet_01v8 L={L} W={W} nf=1 ad='int((nf+1)/2) * W/nf * 0.29'
+ as='int((nf+2)/2) * W/nf * 0.29' pd='2*int((nf+1)/2) * (W/nf + 0.29)' ps='2*int((nf+2)/2) * (W/nf + 0.29)'
+ nrd='0.29 / W' nrs='0.29 / W' sa=0 sb=0 sd=0 mult=1 m=1
XM100 GND net37 net31 GND sky130_fd_pr__nfet_01v8 L={L} W={W} nf=1 ad='int((nf+1)/2) * W/nf * 0.29' as='int((nf+2)/2) * W/nf * 0.29'
+ pd='2*int((nf+1)/2) * (W/nf + 0.29)' ps='2*int((nf+2)/2) * (W/nf + 0.29)' nrd='0.29 / W' nrs='0.29 / W'
+ sa=0 sb=0 sd=0 mult=1 m=1
XM101 net33 net15 net30 GND sky130_fd_pr__nfet_01v8 L={L} W={W} nf=1 ad='int((nf+1)/2) * W/nf * 0.29'
+ as='int((nf+2)/2) * W/nf * 0.29' pd='2*int((nf+1)/2) * (W/nf + 0.29)' ps='2*int((nf+2)/2) * (W/nf + 0.29)'
+ nrd='0.29 / W' nrs='0.29 / W' sa=0 sb=0 sd=0 mult=1 m=1
XM102 net30 net15 net33 GND sky130_fd_pr__nfet_01v8 L={L} W={W} nf=1 ad='int((nf+1)/2) * W/nf * 0.29'
+ as='int((nf+2)/2) * W/nf * 0.29' pd='2*int((nf+1)/2) * (W/nf + 0.29)' ps='2*int((nf+2)/2) * (W/nf + 0.29)'
+ nrd='0.29 / W' nrs='0.29 / W' sa=0 sb=0 sd=0 mult=1 m=1
XM103 net29 net15 net30 GND sky130_fd_pr__nfet_01v8 L={L} W={W} nf=1 ad='int((nf+1)/2) * W/nf * 0.29'
+ as='int((nf+2)/2) * W/nf * 0.29' pd='2*int((nf+1)/2) * (W/nf + 0.29)' ps='2*int((nf+2)/2) * (W/nf + 0.29)'
+ nrd='0.29 / W' nrs='0.29 / W' sa=0 sb=0 sd=0 mult=1 m=1
XM104 net33 net15 net29 GND sky130_fd_pr__nfet_01v8 L={L} W={W} nf=1 ad='int((nf+1)/2) * W/nf * 0.29'
+ as='int((nf+2)/2) * W/nf * 0.29' pd='2*int((nf+1)/2) * (W/nf + 0.29)' ps='2*int((nf+2)/2) * (W/nf + 0.29)'
+ nrd='0.29 / W' nrs='0.29 / W' sa=0 sb=0 sd=0 mult=1 m=1
XM105 net32 net15 net33 GND sky130_fd_pr__nfet_01v8 L={L} W={W} nf=1 ad='int((nf+1)/2) * W/nf * 0.29'
+ as='int((nf+2)/2) * W/nf * 0.29' pd='2*int((nf+1)/2) * (W/nf + 0.29)' ps='2*int((nf+2)/2) * (W/nf + 0.29)'
+ nrd='0.29 / W' nrs='0.29 / W' sa=0 sb=0 sd=0 mult=1 m=1
XM106 net33 net15 net32 GND sky130_fd_pr__nfet_01v8 L={L} W={W} nf=1 ad='int((nf+1)/2) * W/nf * 0.29'
+ as='int((nf+2)/2) * W/nf * 0.29' pd='2*int((nf+1)/2) * (W/nf + 0.29)' ps='2*int((nf+2)/2) * (W/nf + 0.29)'
+ nrd='0.29 / W' nrs='0.29 / W' sa=0 sb=0 sd=0 mult=1 m=1
XM107 net33 net38 GND GND sky130_fd_pr__nfet_01v8 L={L} W={W} nf=1 ad='int((nf+1)/2) * W/nf * 0.29' as='int((nf+2)/2) * W/nf * 0.29'
+ pd='2*int((nf+1)/2) * (W/nf + 0.29)' ps='2*int((nf+2)/2) * (W/nf + 0.29)' nrd='0.29 / W' nrs='0.29 / W'
+ sa=0 sb=0 sd=0 mult=1 m=1
XM108 net34 net15 net35 GND sky130_fd_pr__nfet_01v8 L={L} W={W} nf=1 ad='int((nf+1)/2) * W/nf * 0.29'
+ as='int((nf+2)/2) * W/nf * 0.29' pd='2*int((nf+1)/2) * (W/nf + 0.29)' ps='2*int((nf+2)/2) * (W/nf + 0.29)'
+ nrd='0.29 / W' nrs='0.29 / W' sa=0 sb=0 sd=0 mult=1 m=1
XM109 net35 net15 net34 GND sky130_fd_pr__nfet_01v8 L={L} W={W} nf=1 ad='int((nf+1)/2) * W/nf * 0.29'
+ as='int((nf+2)/2) * W/nf * 0.29' pd='2*int((nf+1)/2) * (W/nf + 0.29)' ps='2*int((nf+2)/2) * (W/nf + 0.29)'
+ nrd='0.29 / W' nrs='0.29 / W' sa=0 sb=0 sd=0 mult=1 m=1
XM110 net30 net15 net35 GND sky130_fd_pr__nfet_01v8 L={L} W={W} nf=1 ad='int((nf+1)/2) * W/nf * 0.29'
+ as='int((nf+2)/2) * W/nf * 0.29' pd='2*int((nf+1)/2) * (W/nf + 0.29)' ps='2*int((nf+2)/2) * (W/nf + 0.29)'
+ nrd='0.29 / W' nrs='0.29 / W' sa=0 sb=0 sd=0 mult=1 m=1
XM111 net35 net15 net30 GND sky130_fd_pr__nfet_01v8 L={L} W={W} nf=1 ad='int((nf+1)/2) * W/nf * 0.29'
+ as='int((nf+2)/2) * W/nf * 0.29' pd='2*int((nf+1)/2) * (W/nf + 0.29)' ps='2*int((nf+2)/2) * (W/nf + 0.29)'
+ nrd='0.29 / W' nrs='0.29 / W' sa=0 sb=0 sd=0 mult=1 m=1
XM112 net35 b6out GND GND sky130_fd_pr__nfet_01v8 L={L} W={W} nf=1 ad='int((nf+1)/2) * W/nf * 0.29' as='int((nf+2)/2) * W/nf * 0.29'
+ pd='2*int((nf+1)/2) * (W/nf + 0.29)' ps='2*int((nf+2)/2) * (W/nf + 0.29)' nrd='0.29 / W' nrs='0.29 / W'
+ sa=0 sb=0 sd=0 mult=1 m=1
XM113 GND net39 net32 GND sky130_fd_pr__nfet_01v8 L={L} W={W} nf=1 ad='int((nf+1)/2) * W/nf * 0.29' as='int((nf+2)/2) * W/nf * 0.29'
+ pd='2*int((nf+1)/2) * (W/nf + 0.29)' ps='2*int((nf+2)/2) * (W/nf + 0.29)' nrd='0.29 / W' nrs='0.29 / W'
+ sa=0 sb=0 sd=0 mult=1 m=1
XM114 net29 net15 net32 GND sky130_fd_pr__nfet_01v8 L={L} W={W} nf=1 ad='int((nf+1)/2) * W/nf * 0.29'
+ as='int((nf+2)/2) * W/nf * 0.29' pd='2*int((nf+1)/2) * (W/nf + 0.29)' ps='2*int((nf+2)/2) * (W/nf + 0.29)'
+ nrd='0.29 / W' nrs='0.29 / W' sa=0 sb=0 sd=0 mult=1 m=1
XM115 VDD net29 net29 VDD sky130_fd_pr__pfet_01v8 L={L} W={W} nf=1 ad='int((nf+1)/2) * W/nf * 0.29' as='int((nf+2)/2) * W/nf * 0.29'
+ pd='2*int((nf+1)/2) * (W/nf + 0.29)' ps='2*int((nf+2)/2) * (W/nf + 0.29)' nrd='0.29 / W' nrs='0.29 / W'
+ sa=0 sb=0 sd=0 mult=1 m=1
**** begin user architecture code

.option wnflag=1
.param MC_SWITCH=1.0
.lib ~/skywater/skywater-pdk/libraries/sky130_fd_pr_ngspice/latest/models/sky130.lib.spice tt


.param W=24
.param L=1
.control
  set wr_singlescale
  let runs = 10
  let run = 1
  while run <= runs
    set appendwrite = FALSE
    set wr_vecnames
    let code = 0
    while code < 128
      if code eq 0
        let b0 = 0
      else
        let b0 = code % 2 * 1.8
      end
      if floor(code / 2) eq 0
        let b1 = 0
      else
        let b1 = floor(code / 2) % 2 * 1.8
      end
      if floor(code / 4) eq 0
        let b2 = 0
      else
        let b2 = floor(code / 4) % 2 * 1.8
      end
      if floor(code / 8) eq 0
        let b3 = 0
      else
        let b3 = floor(code / 8) % 2 * 1.8
      end
      if floor(code / 16) eq 0
        let b4 = 0
      else
        let b4 = floor(code / 16) % 2 * 1.8
      end
      if floor(code / 32) eq 0
        let b5 = 0
      else
        let b5 = floor(code / 32) % 2 * 1.8
      end
      if floor(code / 64) eq 0
        let b6 = 0
      else
        let b6 = floor(code / 64) % 2 * 1.8
      end
      alter v0 $&b0
      alter v1 $&b1
      alter v2 $&b2
      alter v3 $&b3
      alter v4 $&b4
      alter v5 $&b5
      alter v6 $&b6
      save all
      op
      wrdata ~/Documents/current-output-dac-vlsi/simulations/{$&run}.txt v(Vbn) i(Vout) i(Vout1) v(b6)
+ v(b5) v(b4) v(b3) v(b2) v(b1) v(b0) v(b0out) v(b1out) v(b6out)
      if code eq 0
        set appendwrite
        set wr_vecnames = FALSE
      end
      let code = code + 1
    end
    reset
    let run = run + 1
  end
  quit
.endc

**** end user architecture code
**.ends

* expanding   symbol:  /home/madvlsi/Documents/current-output-dac-vlsi/schematics/mux.sym # of
*+ pins=4
** sym_path: dac/schematics/mux.sym
** sch_path: dac/schematics/mux.sch
.subckt mux A B Y S
*.ipin A
*.ipin B
*.ipin S
*.opin Y
XM1 A S Y VDD sky130_fd_pr__pfet_01v8 L=0.15 W=1 nf=1 ad='int((nf+1)/2) * W/nf * 0.29' as='int((nf+2)/2) * W/nf * 0.29'
+ pd='2*int((nf+1)/2) * (W/nf + 0.29)' ps='2*int((nf+2)/2) * (W/nf + 0.29)' nrd='0.29 / W' nrs='0.29 / W'
+ sa=0 sb=0 sd=0 mult=1 m=1
XM3 net1 S VDD VDD sky130_fd_pr__pfet_01v8 L=0.15 W=1 nf=1 ad='int((nf+1)/2) * W/nf * 0.29' as='int((nf+2)/2) * W/nf * 0.29'
+ pd='2*int((nf+1)/2) * (W/nf + 0.29)' ps='2*int((nf+2)/2) * (W/nf + 0.29)' nrd='0.29 / W' nrs='0.29 / W'
+ sa=0 sb=0 sd=0 mult=1 m=1
XM4 net1 S GND GND sky130_fd_pr__nfet_01v8 L=0.15 W=1 nf=1 ad='int((nf+1)/2) * W/nf * 0.29' as='int((nf+2)/2) * W/nf * 0.29'
+ pd='2*int((nf+1)/2) * (W/nf + 0.29)' ps='2*int((nf+2)/2) * (W/nf + 0.29)' nrd='0.29 / W' nrs='0.29 / W'
+ sa=0 sb=0 sd=0 mult=1 m=1
XM5 A net1 Y GND sky130_fd_pr__nfet_01v8 L=0.15 W=1 nf=1 ad='int((nf+1)/2) * W/nf * 0.29' as='int((nf+2)/2) * W/nf * 0.29'
+ pd='2*int((nf+1)/2) * (W/nf + 0.29)' ps='2*int((nf+2)/2) * (W/nf + 0.29)' nrd='0.29 / W' nrs='0.29 / W'
+ sa=0 sb=0 sd=0 mult=1 m=1
XM2 B net1 Y VDD sky130_fd_pr__pfet_01v8 L=0.15 W=1 nf=1 ad='int((nf+1)/2) * W/nf * 0.29' as='int((nf+2)/2) * W/nf * 0.29'
+ pd='2*int((nf+1)/2) * (W/nf + 0.29)' ps='2*int((nf+2)/2) * (W/nf + 0.29)' nrd='0.29 / W' nrs='0.29 / W'
+ sa=0 sb=0 sd=0 mult=1 m=1
XM6 B S Y GND sky130_fd_pr__nfet_01v8 L=0.15 W=1 nf=1 ad='int((nf+1)/2) * W/nf * 0.29' as='int((nf+2)/2) * W/nf * 0.29'
+ pd='2*int((nf+1)/2) * (W/nf + 0.29)' ps='2*int((nf+2)/2) * (W/nf + 0.29)' nrd='0.29 / W' nrs='0.29 / W'
+ sa=0 sb=0 sd=0 mult=1 m=1
.ends

.GLOBAL GND
.GLOBAL VDD
.end
